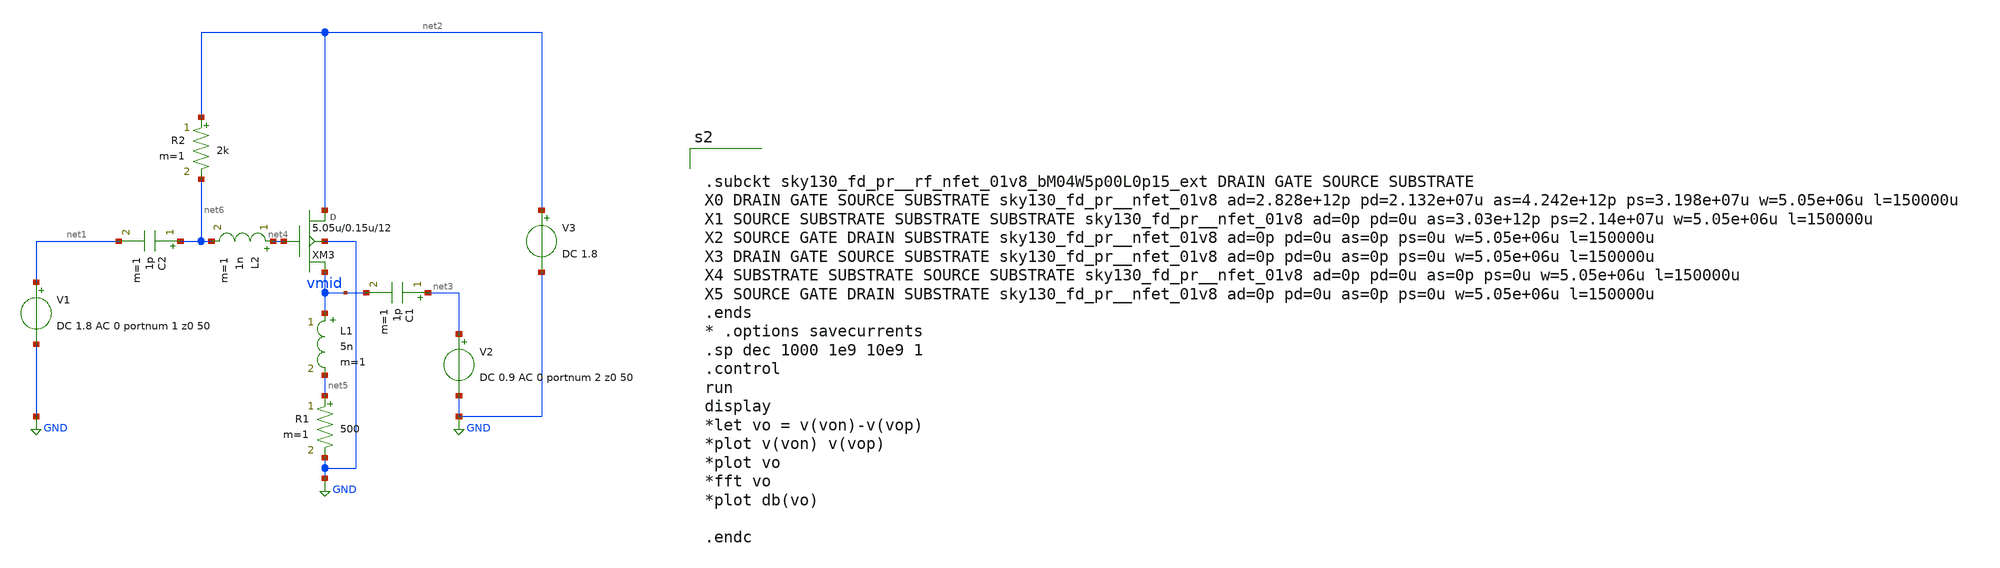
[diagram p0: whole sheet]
** sch_path: xschem/untitled-6.sch
**.subckt untitled-6
XM3 net2 net4 vmid GND sky130_fd_pr__rf_nfet_01v8_bM04W5p00L0p15_ext w=5.05u l=0.15u m=12
V2 net3 GND DC 0.9 AC 0 portnum 2 z0 50
V1 net1 GND DC 1.8 AC 0 portnum 1 z0 50
L1 vmid net5 5n m=1
V3 net2 GND DC 1.8
C1 net3 vmid 1p m=1
L2 net4 net6 1n m=1
R1 net5 GND 500 m=1
C2 net6 net1 1p m=1
R2 net2 net6 2k m=1
**** begin user architecture code


.subckt sky130_fd_pr__rf_nfet_01v8_bM04W5p00L0p15_ext DRAIN GATE SOURCE SUBSTRATE
X0 DRAIN GATE SOURCE SUBSTRATE sky130_fd_pr__nfet_01v8 ad=2.828e+12p pd=2.132e+07u as=4.242e+12p
+ ps=3.198e+07u w=5.05e+06u l=150000u
X1 SOURCE SUBSTRATE SUBSTRATE SUBSTRATE sky130_fd_pr__nfet_01v8 ad=0p pd=0u as=3.03e+12p
+ ps=2.14e+07u w=5.05e+06u l=150000u
X2 SOURCE GATE DRAIN SUBSTRATE sky130_fd_pr__nfet_01v8 ad=0p pd=0u as=0p ps=0u w=5.05e+06u l=150000u
X3 DRAIN GATE SOURCE SUBSTRATE sky130_fd_pr__nfet_01v8 ad=0p pd=0u as=0p ps=0u w=5.05e+06u l=150000u
X4 SUBSTRATE SUBSTRATE SOURCE SUBSTRATE sky130_fd_pr__nfet_01v8 ad=0p pd=0u as=0p ps=0u w=5.05e+06u
+ l=150000u
X5 SOURCE GATE DRAIN SUBSTRATE sky130_fd_pr__nfet_01v8 ad=0p pd=0u as=0p ps=0u w=5.05e+06u l=150000u
.ends
* .options savecurrents
.sp dec 1000 1e9 10e9 1
.control
run
display
*let vo = v(von)-v(vop)
*plot v(von) v(vop)
*plot vo
*fft vo
*plot db(vo)

.endc


.lib $::SKYWATER_MODELS/sky130.lib.spice tt
* .include $::PDKPATH/libs.ref/sky130_fd_sc_hvl/spice/sky130_fd_sc_hvl.spice

**** end user architecture code
**.ends
.GLOBAL GND
.end
